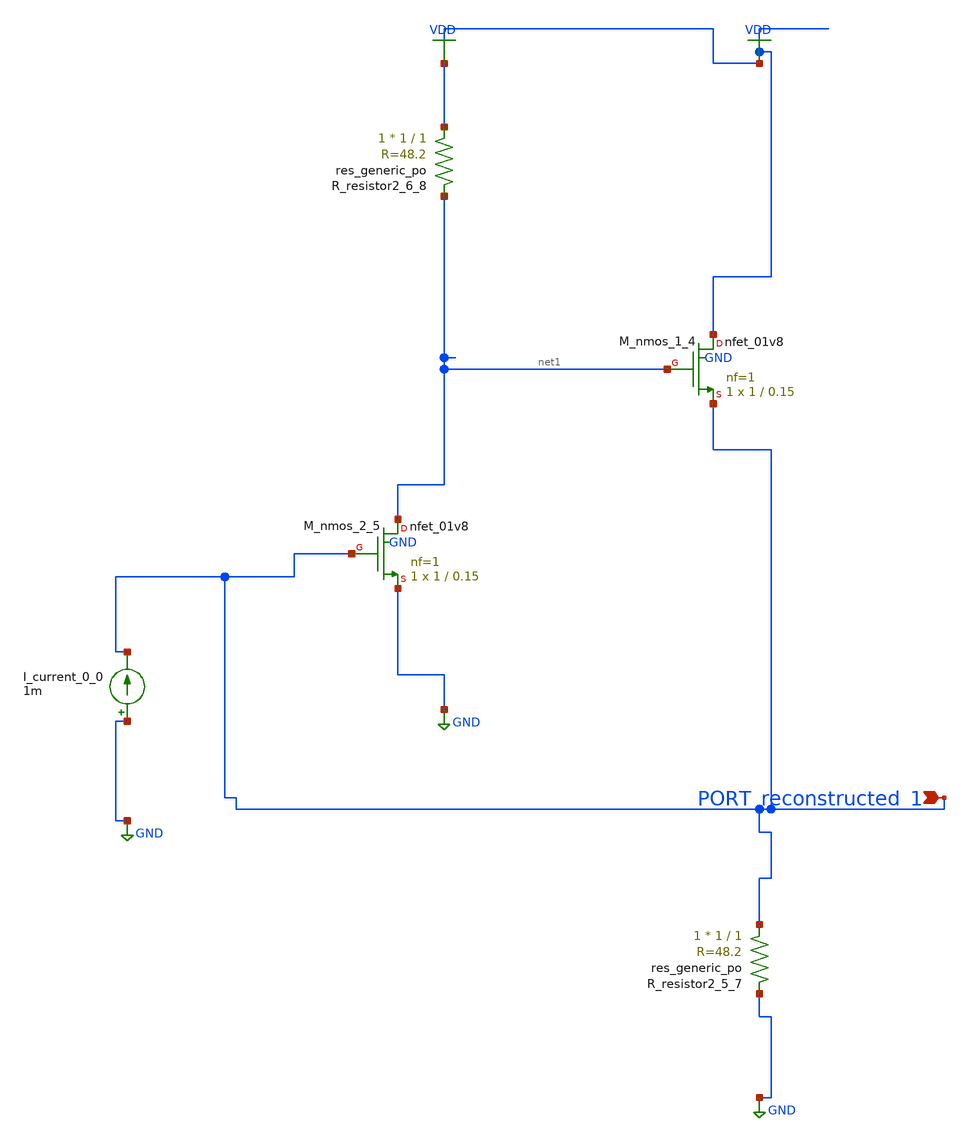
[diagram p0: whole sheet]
** sch_path: schematics/AMSNet/589.sch
**.subckt 589 PORT_reconstructed_1
*.ipin PORT_reconstructed_1
I_current_0_0 GND PORT_reconstructed_1 1m
XM_nmos_1_4 VDD net1 PORT_reconstructed_1 GND sky130_fd_pr__nfet_01v8 L=0.15 W=1 nf=1 ad='int((1 + 1)/2) * 1 / 1 * 0.29'
+ as='int((1 + 2)/2) * 1 / 1 * 0.29' pd='2*int((1 + 1)/2) * (1 / 1 + 0.29)' ps='2*int((1 + 2)/2) * (1 / 1 + 0.29)'
+ nrd='0.29 / 1 ' nrs='0.29 / 1 ' sa=0 sb=0 sd=0 mult=1 m=1
XM_nmos_2_5 net1 PORT_reconstructed_1 GND GND sky130_fd_pr__nfet_01v8 L=0.15 W=1 nf=1 ad='int((1 + 1)/2) * 1 / 1 * 0.29'
+ as='int((1 + 2)/2) * 1 / 1 * 0.29' pd='2*int((1 + 1)/2) * (1 / 1 + 0.29)' ps='2*int((1 + 2)/2) * (1 / 1 + 0.29)'
+ nrd='0.29 / 1 ' nrs='0.29 / 1 ' sa=0 sb=0 sd=0 mult=1 m=1
XR_resistor2_5_7 PORT_reconstructed_1 GND sky130_fd_pr__res_generic_po W=1 L=1 m=1
XR_resistor2_6_8 VDD net1 sky130_fd_pr__res_generic_po W=1 L=1 m=1
**.ends
.GLOBAL GND
.GLOBAL VDD
.end
